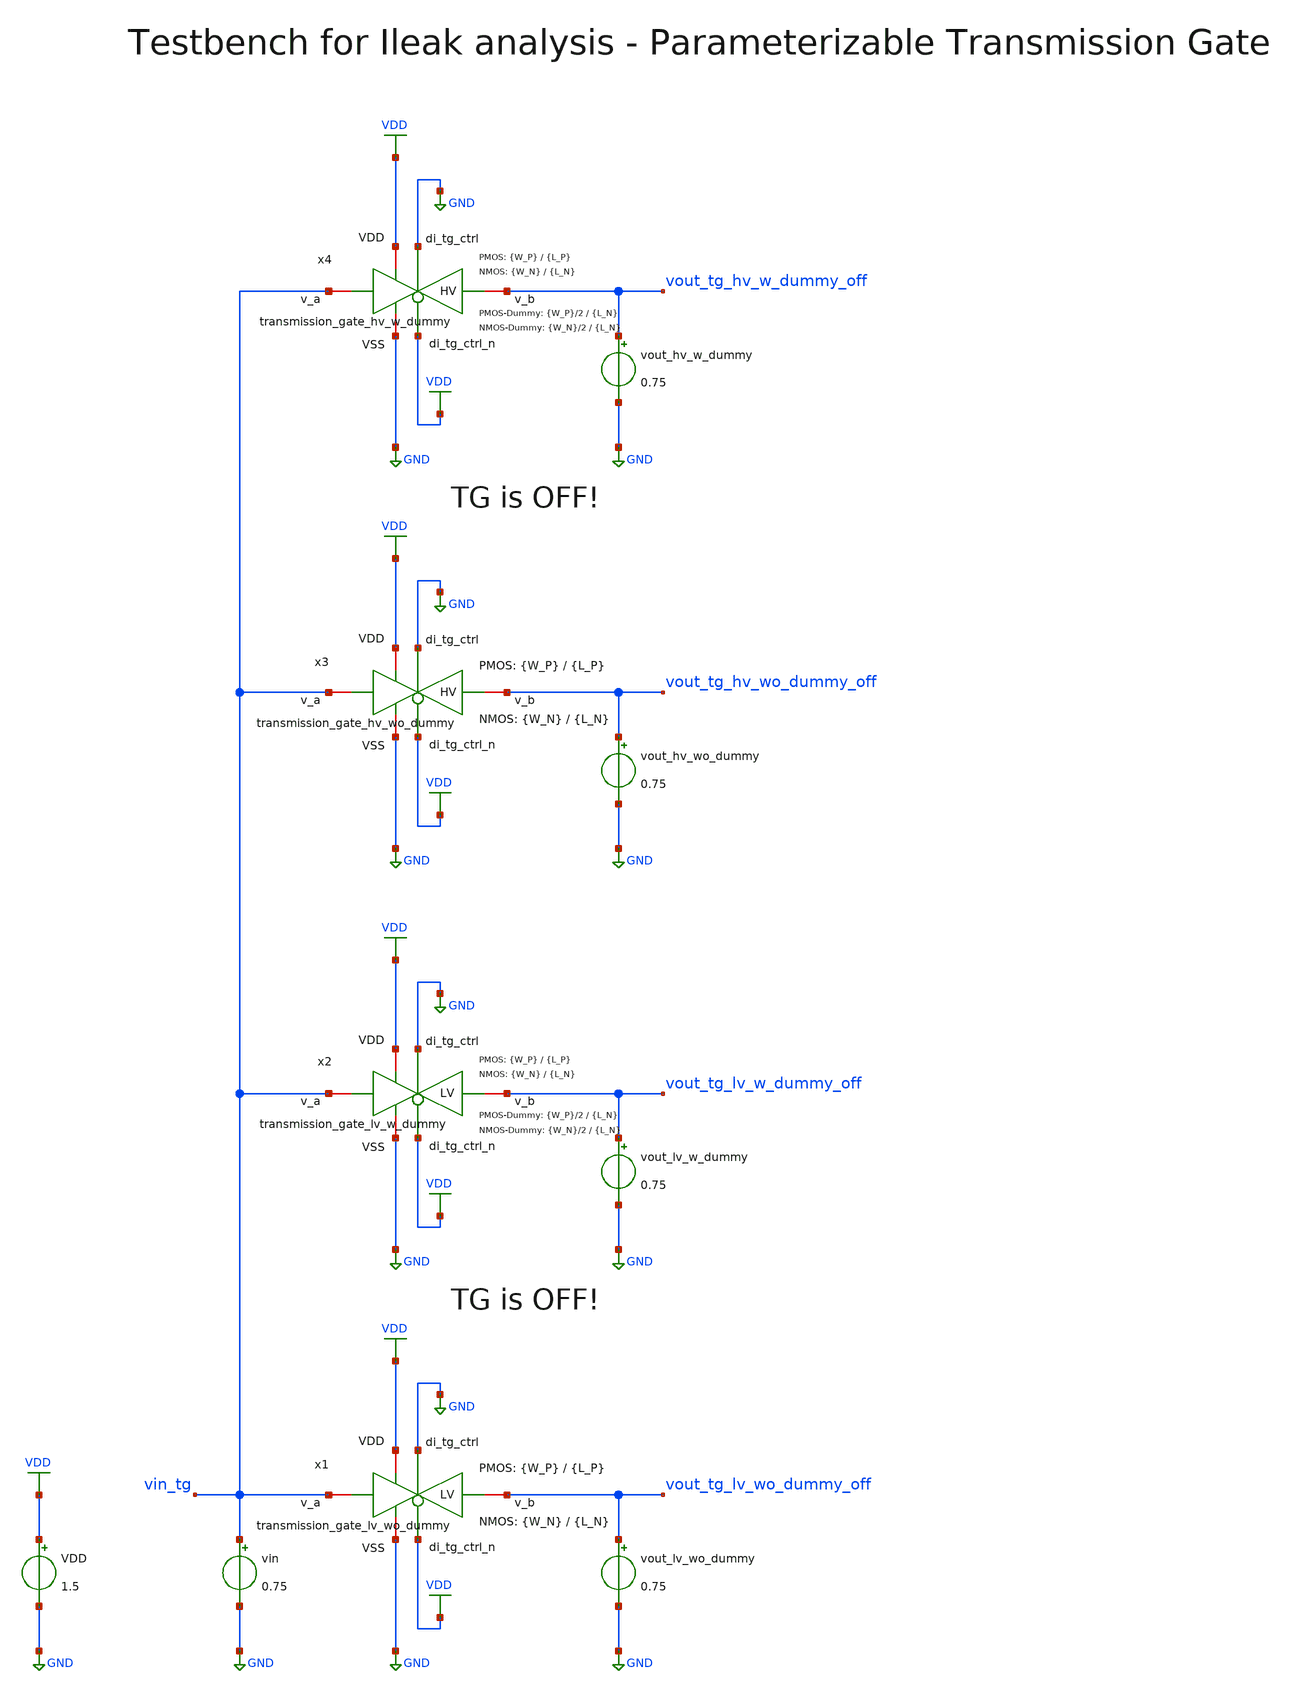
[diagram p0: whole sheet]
** sch_path: SG13G2_ATBS-ADC-main/xschem/transmission_gate/testbenches/transmission_gate_tb_dc_Ileak.sch
**.subckt transmission_gate_tb_dc_Ileak
VDD VDD GND 1.5
vin vin_tg GND 0.75
vout_lv_wo_dummy vout_tg_lv_wo_dummy_off GND 0.75
vout_lv_w_dummy vout_tg_lv_w_dummy_off GND 0.75
vout_hv_wo_dummy vout_tg_hv_wo_dummy_off GND 0.75
vout_hv_w_dummy vout_tg_hv_w_dummy_off GND 0.75
x1 VDD GND GND vout_tg_lv_wo_dummy_off vin_tg VDD transmission_gate_lv_wo_dummy W_P={W_P} L_P={L_P} W_N={W_N}
+ L_N={L_N}
x2 VDD GND GND vout_tg_lv_w_dummy_off vin_tg VDD transmission_gate_lv_w_dummy W_P={W_P} L_P={L_P} W_N={W_N}
+ L_N={L_N} W_P_D={W_P}/2 L_P_D={L_N} W_N_D={W_N}/2 L_N_D={L_N}
x3 VDD GND GND vout_tg_hv_wo_dummy_off vin_tg VDD transmission_gate_hv_wo_dummy W_P={W_P} L_P={L_P} W_N={W_N}
+ L_N={L_N}
x4 VDD GND GND vout_tg_hv_w_dummy_off vin_tg VDD transmission_gate_hv_w_dummy W_P={W_P} L_P={L_P} W_N={W_N}
+ L_N={L_N} W_P_D={W_P}/2 L_P_D={L_N} W_N_D={W_N}/2 L_N_D={L_N}
**** begin user architecture code

.lib cornerMOShv.lib mos_tt
.lib cornerMOSlv.lib mos_tt
.lib cornerRES.lib res_typ



.param temp=27
.param W_N=1u
.param L_N=0.5u
.param W_P=1u
.param L_P=0.5u
.options savecurrents
.control

save all

* Operating Point Analysis
op
remzerovec
write transmission_gate_tb_dc_Ileak.raw
set appendwrite
* =======================================

* DC Sweep Analysis LV with Dummy
dc vin 0 1.5 10m vout_lv_w_dummy 0 1.5 0.75
write transmission_gate_tb_dc_Ileak.raw
set appendwrite

* Off-Leakage Current
let Ileak_lv_w_dummy = i(vout_lv_w_dummy)
plot Ileak_lv_w_dummy
* =======================================

* DC Sweep Analysis HV with Dummy
dc vin 0 1.5 10m vout_hv_w_dummy 0 1.5 0.75
write transmission_gate_tb_dc_Ileak.raw
set appendwrite

* Off-Leakage Current
let Ileak_hv_w_dummy = i(vout_hv_w_dummy)
plot Ileak_hv_w_dummy
* =======================================

* DC Sweep Analysis LV without Dummy
dc vin 0 1.5 10m vout_lv_wo_dummy 0 1.5 0.75
write transmission_gate_tb_dc_Ileak.raw
set appendwrite

* Off-Leakage Current
let Ileak_lv_wo_dummy = i(vout_lv_wo_dummy)
plot Ileak_lv_wo_dummy
* =======================================

* DC Sweep Analysis HV without Dummy
dc vin 0 1.5 10m vout_hv_wo_dummy 0 1.5 0.75
write transmission_gate_tb_dc_Ileak.raw

* Off-Leakage Current
let Ileak_hv_wo_dummy = i(vout_hv_wo_dummy)
plot Ileak_hv_wo_dummy
* =======================================

* Writing Data
set wr_singlescale
set wr_vecnames
let Ileak_lv_w_dummy = dc1.Ileak_lv_w_dummy
let Ileak_hv_w_dummy = dc2.Ileak_hv_w_dummy
let Ileak_lv_wo_dummy = dc3.Ileak_lv_wo_dummy
let Ileak_hv_wo_dummy = dc4.Ileak_hv_wo_dummy
wrdata
+ /foss/designs/SG13G2_ATBS-ADC-main/python/plot_simulations/data/transmission_gate_tb_dc_Ileak.txt v(Ileak_lv_w_dummy) v(Ileak_hv_w_dummy) v(Ileak_lv_wo_dummy) v(Ileak_hv_wo_dummy)
* =======================================

*quit
.endc

**** end user architecture code
**.ends

* expanding   symbol:  transmission_gate/transmission_gate_lv_wo_dummy.sym # of pins=6
** sym_path: SG13G2_ATBS-ADC-main/xschem/transmission_gate/transmission_gate_lv_wo_dummy.sym
** sch_path: SG13G2_ATBS-ADC-main/xschem/transmission_gate/transmission_gate_lv_wo_dummy.sch
.subckt transmission_gate_lv_wo_dummy VDD di_tg_ctrl VSS v_b v_a di_tg_ctrl_n  W_P=1.0u L_P=0.13u
+ W_N=1.0u L_N=0.13u
*.iopin v_a
*.iopin v_b
*.iopin VDD
*.iopin VSS
*.ipin di_tg_ctrl
*.ipin di_tg_ctrl_n
XM1 v_a di_tg_ctrl v_b VSS sg13_lv_nmos w=W_N l=L_N ng=1 m=1 mm_ok=1
XM2 v_a di_tg_ctrl_n v_b VDD sg13_lv_pmos w=W_P l=L_P ng=1 m=1 mm_ok=1
.ends


* expanding   symbol:  transmission_gate/transmission_gate_lv_w_dummy.sym # of pins=6
** sym_path: SG13G2_ATBS-ADC-main/xschem/transmission_gate/transmission_gate_lv_w_dummy.sym
** sch_path: SG13G2_ATBS-ADC-main/xschem/transmission_gate/transmission_gate_lv_w_dummy.sch
.subckt transmission_gate_lv_w_dummy VDD di_tg_ctrl VSS v_b v_a di_tg_ctrl_n  W_P=2.0u L_P=0.13u
+ W_N=2.0u L_N=0.13u W_P_D=1.0u L_P_D=0.13u W_N_D=1.0u L_N_D=0.13u
*.iopin v_a
*.iopin v_b
*.iopin VDD
*.iopin VSS
*.ipin di_tg_ctrl
*.ipin di_tg_ctrl_n
XM1 v_a di_tg_ctrl v_b VSS sg13_lv_nmos w=W_N l=L_N ng=1 m=1 mm_ok=1
XM2 v_a di_tg_ctrl_n v_b VDD sg13_lv_pmos w=W_P l=L_P ng=1 m=1 mm_ok=1
XMdummy2 v_b di_tg_ctrl v_b VDD sg13_lv_pmos w=W_P_D l=L_P_D ng=1 m=1 mm_ok=1
XMdummy1 v_b di_tg_ctrl_n v_b VSS sg13_lv_nmos w=W_N_D l=L_N_D ng=1 m=1 mm_ok=1
.ends


* expanding   symbol:  transmission_gate/transmission_gate_hv_wo_dummy.sym # of pins=6
** sym_path: SG13G2_ATBS-ADC-main/xschem/transmission_gate/transmission_gate_hv_wo_dummy.sym
** sch_path: SG13G2_ATBS-ADC-main/xschem/transmission_gate/transmission_gate_hv_wo_dummy.sch
.subckt transmission_gate_hv_wo_dummy VDD di_tg_ctrl VSS v_b v_a di_tg_ctrl_n  W_P=1.0u L_P=0.5u
+ W_N=1.0u L_N=0.5u
*.iopin v_a
*.iopin v_b
*.iopin VDD
*.iopin VSS
*.ipin di_tg_ctrl
*.ipin di_tg_ctrl_n
XM1 v_a di_tg_ctrl v_b VSS sg13_hv_nmos w=W_N l=L_N ng=1 m=1 mm_ok=1
XM2 v_a di_tg_ctrl_n v_b VDD sg13_hv_pmos w=W_P l=L_P ng=1 m=1 mm_ok=1
.ends


* expanding   symbol:  transmission_gate/transmission_gate_hv_w_dummy.sym # of pins=6
** sym_path: SG13G2_ATBS-ADC-main/xschem/transmission_gate/transmission_gate_hv_w_dummy.sym
** sch_path: SG13G2_ATBS-ADC-main/xschem/transmission_gate/transmission_gate_hv_w_dummy.sch
.subckt transmission_gate_hv_w_dummy VDD di_tg_ctrl VSS v_b v_a di_tg_ctrl_n  W_P=2.0u L_P=0.5u
+ W_N=2.0u L_N=0.5u W_P_D=1.0u L_P_D=0.5u W_N_D=1.0u L_N_D=0.5u
*.iopin v_a
*.iopin v_b
*.iopin VDD
*.iopin VSS
*.ipin di_tg_ctrl
*.ipin di_tg_ctrl_n
XM1 v_a di_tg_ctrl v_b VSS sg13_hv_nmos w=W_N l=L_N ng=1 m=1 mm_ok=1
XM2 v_a di_tg_ctrl_n v_b VDD sg13_hv_pmos w=W_P l=L_P ng=1 m=1 mm_ok=1
XMdummy1 v_b di_tg_ctrl_n v_b VSS sg13_hv_nmos w=W_N_D l=L_N_D ng=1 m=1 mm_ok=1
XMdummy2 v_b di_tg_ctrl v_b VDD sg13_hv_pmos w=W_P_D l=L_P_D ng=1 m=1 mm_ok=1
.ends

.GLOBAL GND
.GLOBAL VDD
.end
